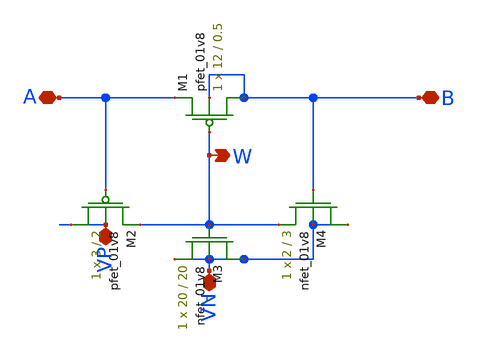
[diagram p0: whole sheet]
** sch_path: schematic/memristor_emulator.sch
**.subckt memristor_emulator VN VP W B A
*.iopin VN
*.iopin VP
*.opin W
*.iopin B
*.iopin A
XM1 B W A B sky130_fd_pr__pfet_01v8 L=0.5 W=12 nf=1 ad='int((nf+1)/2) * W/nf * 0.29' as='int((nf+2)/2) * W/nf * 0.29'
+ pd='2*int((nf+1)/2) * (W/nf + 0.29)' ps='2*int((nf+2)/2) * (W/nf + 0.29)' nrd='0.29 / W' nrs='0.29 / W'
+ sa=0 sb=0 sd=0 mult=1 m=1
XM2 VP A W VP sky130_fd_pr__pfet_01v8 L=2 W=3 nf=1 ad='int((nf+1)/2) * W/nf * 0.29' as='int((nf+2)/2) * W/nf * 0.29'
+ pd='2*int((nf+1)/2) * (W/nf + 0.29)' ps='2*int((nf+2)/2) * (W/nf + 0.29)' nrd='0.29 / W' nrs='0.29 / W'
+ sa=0 sb=0 sd=0 mult=1 m=1
XM3 VN W VN VN sky130_fd_pr__nfet_01v8 L=20 W=20 nf=1 ad='int((nf+1)/2) * W/nf * 0.29' as='int((nf+2)/2) * W/nf * 0.29'
+ pd='2*int((nf+1)/2) * (W/nf + 0.29)' ps='2*int((nf+2)/2) * (W/nf + 0.29)' nrd='0.29 / W' nrs='0.29 / W'
+ sa=0 sb=0 sd=0 mult=1 m=1
XM4 VN B W VN sky130_fd_pr__nfet_01v8 L=3 W=2 nf=1 ad='int((nf+1)/2) * W/nf * 0.29' as='int((nf+2)/2) * W/nf * 0.29'
+ pd='2*int((nf+1)/2) * (W/nf + 0.29)' ps='2*int((nf+2)/2) * (W/nf + 0.29)' nrd='0.29 / W' nrs='0.29 / W'
+ sa=0 sb=0 sd=0 mult=1 m=1
**.ends
.end
